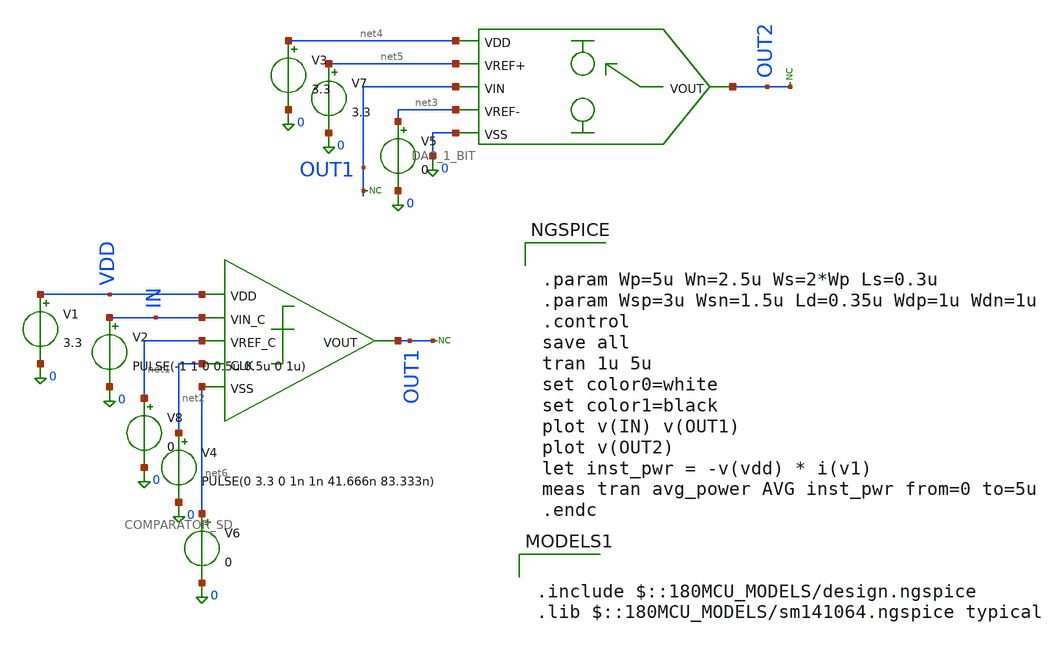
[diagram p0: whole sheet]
** sch_path: src/schematics/INTEGRATION/integrated_comparator_dac.sch
**.subckt integrated_comparator_dac
V2 IN 0 PULSE(-1 1 0 0.5u 0.5u 0 1u)
V4 net2 0 PULSE(0 3.3 0 1n 1n 41.666n 83.333n)
V1 VDD 0 3.3
x1 VDD IN net1 net2 OUT1 net6 COMPARATOR_SD
V3 net4 0 3.3
x2 net4 net5 OUT1 OUT2 net3 0 DAC_1_BIT
V5 net3 0 0
* noconn OUT1
* noconn OUT1
* noconn OUT2
V6 net6 0 0
V8 net1 0 0
V7 net5 0 3.3
**** begin user architecture code

.include $::180MCU_MODELS/design.ngspice
.lib $::180MCU_MODELS/sm141064.ngspice typical



.param Wp=5u Wn=2.5u Ws=2*Wp Ls=0.3u
.param Wsp=3u Wsn=1.5u Ld=0.35u Wdp=1u Wdn=1u
.control
save all
tran 1u 5u
set color0=white
set color1=black
plot v(IN) v(OUT1)
plot v(OUT2)
let inst_pwr = -v(vdd) * i(v1)
meas tran avg_power AVG inst_pwr from=0 to=5u
.endc



**** end user architecture code
**.ends

* expanding   symbol:
*+  /foss/designs/low-power-12b-first-order-delta-sigma-adc/src/schematics/latched comparator/COMPARATOR_SD.sym # of pins=6
** sym_path: src/schematics/latched_comparator/COMPARATOR_SD.sym
** sch_path: src/schematics/latched_comparator/COMPARATOR_SD.sch
.subckt COMPARATOR_SD VDD VIN_C VREF_C CLK VOUT VSS
*.ipin VIN_C
*.ipin VREF_C
*.ipin CLK
*.opin VOUT
*.ipin VDD
*.ipin VSS
XM1 net3 VIN_C net1 VDD pfet_03v3 L=Lc W=Wpc nf=1 ad='int((nf+1)/2) * W/nf * 0.18u' as='int((nf+2)/2) * W/nf * 0.18u'
+ pd='2*int((nf+1)/2) * (W/nf + 0.18u)' ps='2*int((nf+2)/2) * (W/nf + 0.18u)' nrd='0.18u / W' nrs='0.18u / W'
+ sa=0 sb=0 sd=0 m=1
XM2 net5 VREF_C net1 VDD pfet_03v3 L=Lc W=Wpc nf=1 ad='int((nf+1)/2) * W/nf * 0.18u' as='int((nf+2)/2) * W/nf * 0.18u'
+ pd='2*int((nf+1)/2) * (W/nf + 0.18u)' ps='2*int((nf+2)/2) * (W/nf + 0.18u)' nrd='0.18u / W' nrs='0.18u / W'
+ sa=0 sb=0 sd=0 m=1
XM3 VOUT net2 net5 VDD pfet_03v3 L=Lc W=Wpc nf=1 ad='int((nf+1)/2) * W/nf * 0.18u' as='int((nf+2)/2) * W/nf * 0.18u'
+ pd='2*int((nf+1)/2) * (W/nf + 0.18u)' ps='2*int((nf+2)/2) * (W/nf + 0.18u)' nrd='0.18u / W' nrs='0.18u / W'
+ sa=0 sb=0 sd=0 m=1
XM4 net4 net2 net3 VDD pfet_03v3 L=Lc W=Wpc nf=1 ad='int((nf+1)/2) * W/nf * 0.18u' as='int((nf+2)/2) * W/nf * 0.18u'
+ pd='2*int((nf+1)/2) * (W/nf + 0.18u)' ps='2*int((nf+2)/2) * (W/nf + 0.18u)' nrd='0.18u / W' nrs='0.18u / W'
+ sa=0 sb=0 sd=0 m=1
XM6 net2 CLK VDD VDD pfet_03v3 L=Lc W=Wpc nf=1 ad='int((nf+1)/2) * W/nf * 0.18u' as='int((nf+2)/2) * W/nf * 0.18u'
+ pd='2*int((nf+1)/2) * (W/nf + 0.18u)' ps='2*int((nf+2)/2) * (W/nf + 0.18u)' nrd='0.18u / W' nrs='0.18u / W'
+ sa=0 sb=0 sd=0 m=1
XM7 net2 CLK VSS VSS nfet_03v3 L=Lc W=Wnc nf=1 ad='int((nf+1)/2) * W/nf * 0.18u' as='int((nf+2)/2) * W/nf * 0.18u'
+ pd='2*int((nf+1)/2) * (W/nf + 0.18u)' ps='2*int((nf+2)/2) * (W/nf + 0.18u)' nrd='0.18u / W' nrs='0.18u / W'
+ sa=0 sb=0 sd=0 m=1
XM8 net4 CLK VOUT VSS nfet_03v3 L=Lc W=Wnc nf=1 ad='int((nf+1)/2) * W/nf * 0.18u' as='int((nf+2)/2) * W/nf * 0.18u'
+ pd='2*int((nf+1)/2) * (W/nf + 0.18u)' ps='2*int((nf+2)/2) * (W/nf + 0.18u)' nrd='0.18u / W' nrs='0.18u / W'
+ sa=0 sb=0 sd=0 m=1
XM9 net7 VOUT VDD VDD pfet_03v3 L=Lc W=Wpc nf=1 ad='int((nf+1)/2) * W/nf * 0.18u' as='int((nf+2)/2) * W/nf * 0.18u'
+ pd='2*int((nf+1)/2) * (W/nf + 0.18u)' ps='2*int((nf+2)/2) * (W/nf + 0.18u)' nrd='0.18u / W' nrs='0.18u / W'
+ sa=0 sb=0 sd=0 m=1
XM10 net4 CLK net7 VDD pfet_03v3 L=Lc W=Wpc nf=1 ad='int((nf+1)/2) * W/nf * 0.18u' as='int((nf+2)/2) * W/nf * 0.18u'
+ pd='2*int((nf+1)/2) * (W/nf + 0.18u)' ps='2*int((nf+2)/2) * (W/nf + 0.18u)' nrd='0.18u / W' nrs='0.18u / W'
+ sa=0 sb=0 sd=0 m=1
XM11 net4 VOUT VSS VSS nfet_03v3 L=Lc W=Wnc nf=1 ad='int((nf+1)/2) * W/nf * 0.18u' as='int((nf+2)/2) * W/nf * 0.18u'
+ pd='2*int((nf+1)/2) * (W/nf + 0.18u)' ps='2*int((nf+2)/2) * (W/nf + 0.18u)' nrd='0.18u / W' nrs='0.18u / W'
+ sa=0 sb=0 sd=0 m=1
XM12 net6 net4 VDD VDD pfet_03v3 L=Lc W=Wpc nf=1 ad='int((nf+1)/2) * W/nf * 0.18u' as='int((nf+2)/2) * W/nf * 0.18u'
+ pd='2*int((nf+1)/2) * (W/nf + 0.18u)' ps='2*int((nf+2)/2) * (W/nf + 0.18u)' nrd='0.18u / W' nrs='0.18u / W'
+ sa=0 sb=0 sd=0 m=1
XM13 VOUT CLK net6 VDD pfet_03v3 L=Lc W=Wpc nf=1 ad='int((nf+1)/2) * W/nf * 0.18u' as='int((nf+2)/2) * W/nf * 0.18u'
+ pd='2*int((nf+1)/2) * (W/nf + 0.18u)' ps='2*int((nf+2)/2) * (W/nf + 0.18u)' nrd='0.18u / W' nrs='0.18u / W'
+ sa=0 sb=0 sd=0 m=1
XM14 VOUT net4 VSS VSS nfet_03v3 L=Lc W=Wnc nf=1 ad='int((nf+1)/2) * W/nf * 0.18u' as='int((nf+2)/2) * W/nf * 0.18u'
+ pd='2*int((nf+1)/2) * (W/nf + 0.18u)' ps='2*int((nf+2)/2) * (W/nf + 0.18u)' nrd='0.18u / W' nrs='0.18u / W'
+ sa=0 sb=0 sd=0 m=1
XM5 net1 VSS VDD VDD pfet_03v3 L=Lc W=Wsc nf=1 ad='int((nf+1)/2) * W/nf * 0.18u' as='int((nf+2)/2) * W/nf * 0.18u'
+ pd='2*int((nf+1)/2) * (W/nf + 0.18u)' ps='2*int((nf+2)/2) * (W/nf + 0.18u)' nrd='0.18u / W' nrs='0.18u / W'
+ sa=0 sb=0 sd=0 m=1
.ends


* expanding   symbol:  DAC_1_BIT.sym # of pins=6
** sym_path: src/schematics/dac_1bit/DAC_1_BIT.sym
** sch_path: src/schematics/dac_1bit/DAC_1_BIT.sch
.subckt DAC_1_BIT VDD VREF+ VIN VOUT VREF- VSS
*.ipin VIN
*.ipin VREF+
*.ipin VREF-
*.opin VOUT
*.ipin VDD
*.ipin VSS
XM1 net1 net2 VREF+ VSS nfet_03v3 L=Ld W=Wdn nf=2 ad='int((nf+1)/2) * W/nf * 0.18u' as='int((nf+2)/2) * W/nf * 0.18u'
+ pd='2*int((nf+1)/2) * (W/nf + 0.18u)' ps='2*int((nf+2)/2) * (W/nf + 0.18u)' nrd='0.18u / W' nrs='0.18u / W'
+ sa=0 sb=0 sd=0 m=1
XM2 net1 VIN VREF+ VDD pfet_03v3 L=Ld W=Wdp nf=2 ad='int((nf+1)/2) * W/nf * 0.18u' as='int((nf+2)/2) * W/nf * 0.18u'
+ pd='2*int((nf+1)/2) * (W/nf + 0.18u)' ps='2*int((nf+2)/2) * (W/nf + 0.18u)' nrd='0.18u / W' nrs='0.18u / W'
+ sa=0 sb=0 sd=0 m=1
XM3 net1 VIN VREF- VSS nfet_03v3 L=Ld W=Wdn nf=2 ad='int((nf+1)/2) * W/nf * 0.18u' as='int((nf+2)/2) * W/nf * 0.18u'
+ pd='2*int((nf+1)/2) * (W/nf + 0.18u)' ps='2*int((nf+2)/2) * (W/nf + 0.18u)' nrd='0.18u / W' nrs='0.18u / W'
+ sa=0 sb=0 sd=0 m=1
XM4 net1 net2 VREF- VDD pfet_03v3 L=Ld W=Wdp nf=2 ad='int((nf+1)/2) * W/nf * 0.18u' as='int((nf+2)/2) * W/nf * 0.18u'
+ pd='2*int((nf+1)/2) * (W/nf + 0.18u)' ps='2*int((nf+2)/2) * (W/nf + 0.18u)' nrd='0.18u / W' nrs='0.18u / W'
+ sa=0 sb=0 sd=0 m=1
XM5 net2 VIN VDD VDD pfet_03v3 L=Ld W=Wsp nf=1 ad='int((nf+1)/2) * W/nf * 0.18u' as='int((nf+2)/2) * W/nf * 0.18u'
+ pd='2*int((nf+1)/2) * (W/nf + 0.18u)' ps='2*int((nf+2)/2) * (W/nf + 0.18u)' nrd='0.18u / W' nrs='0.18u / W'
+ sa=0 sb=0 sd=0 m=1
XM6 net2 VIN VSS VSS nfet_03v3 L=Ld W=Wsn nf=1 ad='int((nf+1)/2) * W/nf * 0.18u' as='int((nf+2)/2) * W/nf * 0.18u'
+ pd='2*int((nf+1)/2) * (W/nf + 0.18u)' ps='2*int((nf+2)/2) * (W/nf + 0.18u)' nrd='0.18u / W' nrs='0.18u / W'
+ sa=0 sb=0 sd=0 m=1
XM7 VOUT net1 VDD VDD pfet_03v3 L=Ld W=Wsp nf=1 ad='int((nf+1)/2) * W/nf * 0.18u' as='int((nf+2)/2) * W/nf * 0.18u'
+ pd='2*int((nf+1)/2) * (W/nf + 0.18u)' ps='2*int((nf+2)/2) * (W/nf + 0.18u)' nrd='0.18u / W' nrs='0.18u / W'
+ sa=0 sb=0 sd=0 m=1
XM8 VOUT net1 VSS VSS nfet_03v3 L=Ld W=Wsn nf=1 ad='int((nf+1)/2) * W/nf * 0.18u' as='int((nf+2)/2) * W/nf * 0.18u'
+ pd='2*int((nf+1)/2) * (W/nf + 0.18u)' ps='2*int((nf+2)/2) * (W/nf + 0.18u)' nrd='0.18u / W' nrs='0.18u / W'
+ sa=0 sb=0 sd=0 m=1
.ends

.end
